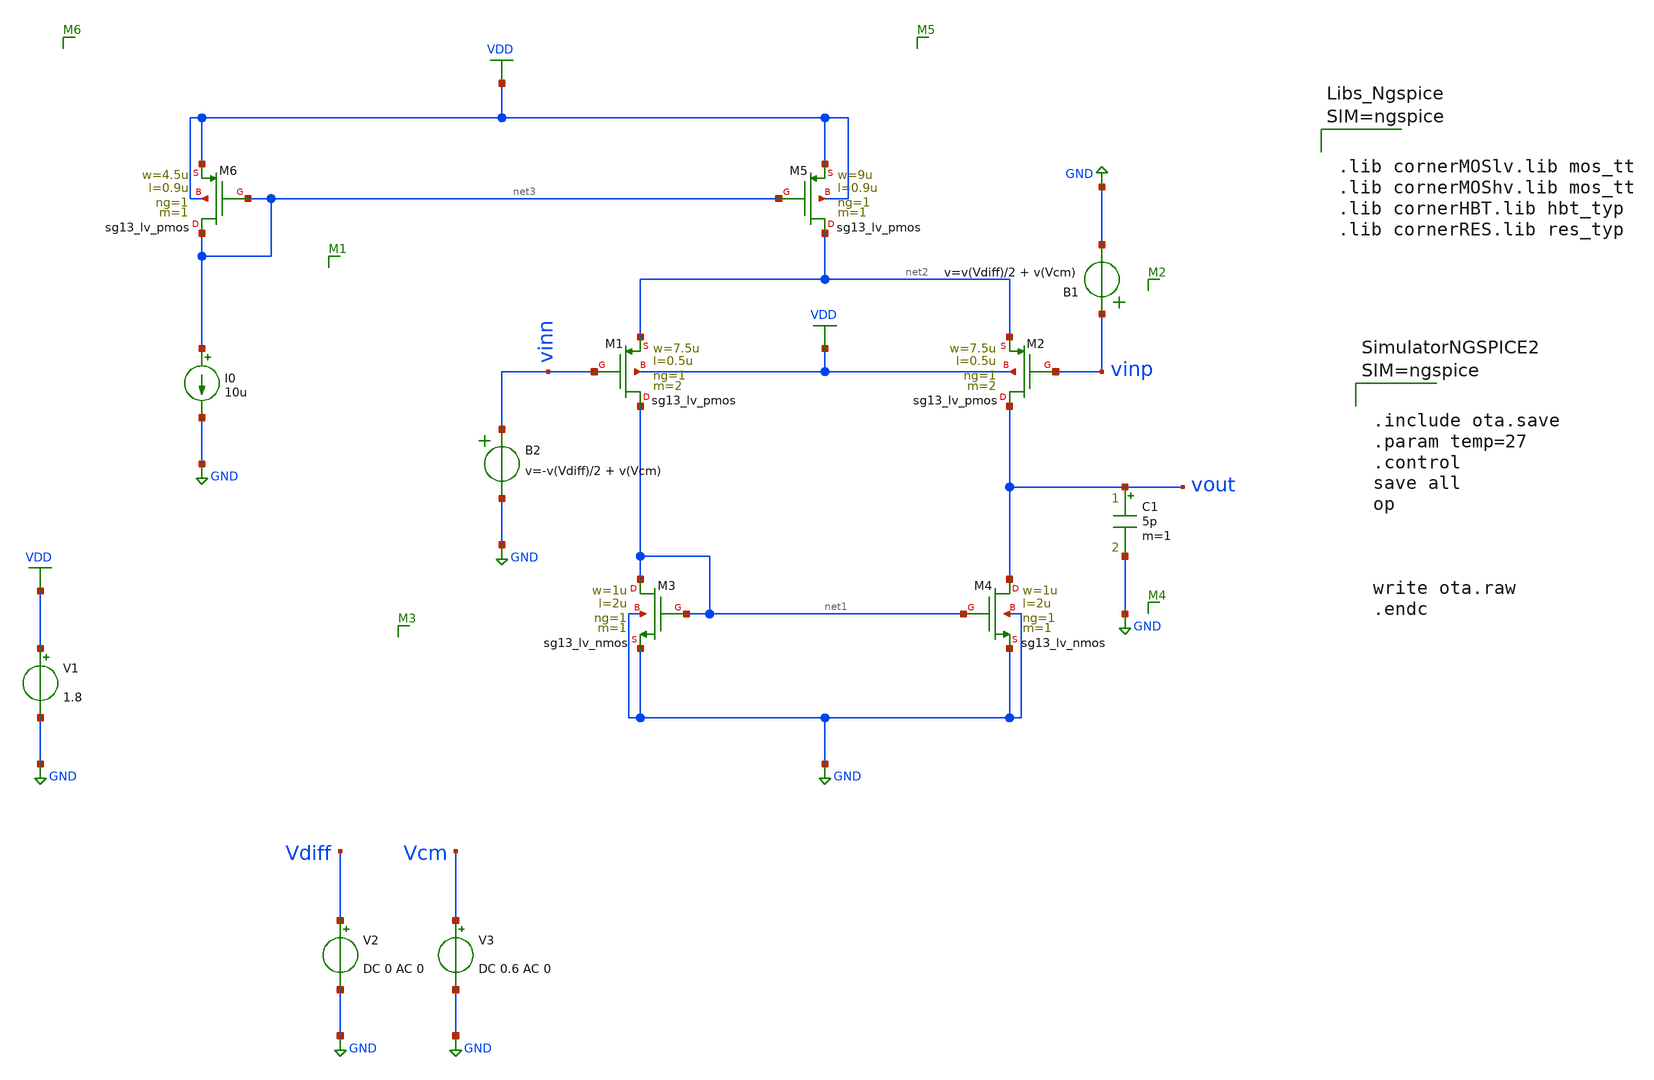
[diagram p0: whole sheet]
** sch_path: Schematics/OTA/ota.sch
**.subckt ota
XM1 net1 vinn net2 VDD sg13_lv_pmos w=7.5u l=0.5u ng=1 m=2 mm_ok=1
XM2 vout vinp net2 VDD sg13_lv_pmos w=7.5u l=0.5u ng=1 m=2 mm_ok=1
XM3 net1 net1 GND GND sg13_lv_nmos w=1u l=2u ng=1 m=1 mm_ok=1
XM4 vout net1 GND GND sg13_lv_nmos w=1u l=2u ng=1 m=1 mm_ok=1
XM5 net2 net3 VDD VDD sg13_lv_pmos w=9u l=0.9u ng=1 m=1 mm_ok=1
XM6 net3 net3 VDD VDD sg13_lv_pmos w=4.5u l=0.9u ng=1 m=1 mm_ok=1
I0 net3 GND 10u
V1 VDD GND 1.8
V2 Vdiff GND DC 0 AC 0
V3 Vcm GND DC 0.6 AC 0
B1 vinp GND v=v(Vdiff)/2 + v(Vcm)
B2 vinn GND v=-v(Vdiff)/2 + v(Vcm)
C1 vout GND 5p m=1
**** begin user architecture code



.lib cornerMOSlv.lib mos_tt
.lib cornerMOShv.lib mos_tt
.lib cornerHBT.lib hbt_typ
.lib cornerRES.lib res_typ






.include ota.save
.param temp=27
.control
save all
op



write ota.raw
.endc



**** end user architecture code
**.ends
.GLOBAL GND
.GLOBAL VDD
.end
